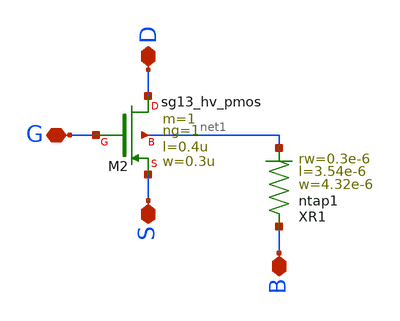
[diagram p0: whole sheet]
** sch_path: LVS-testbenches/schematic/sg13_hv_pmos_ring.sch
**.subckt sg13_hv_pmos_ring D S G B
*.iopin D
*.iopin S
*.iopin G
*.iopin B
XM2 D G S net1 sg13_hv_pmos w=0.3u l=0.4u ng=1 m=1 mm_ok=1
XR1 B net1 ntap1 R=15.7 w=4.32e-6 l=3.54e-6 rw=0.3e-6
**.ends
.end
